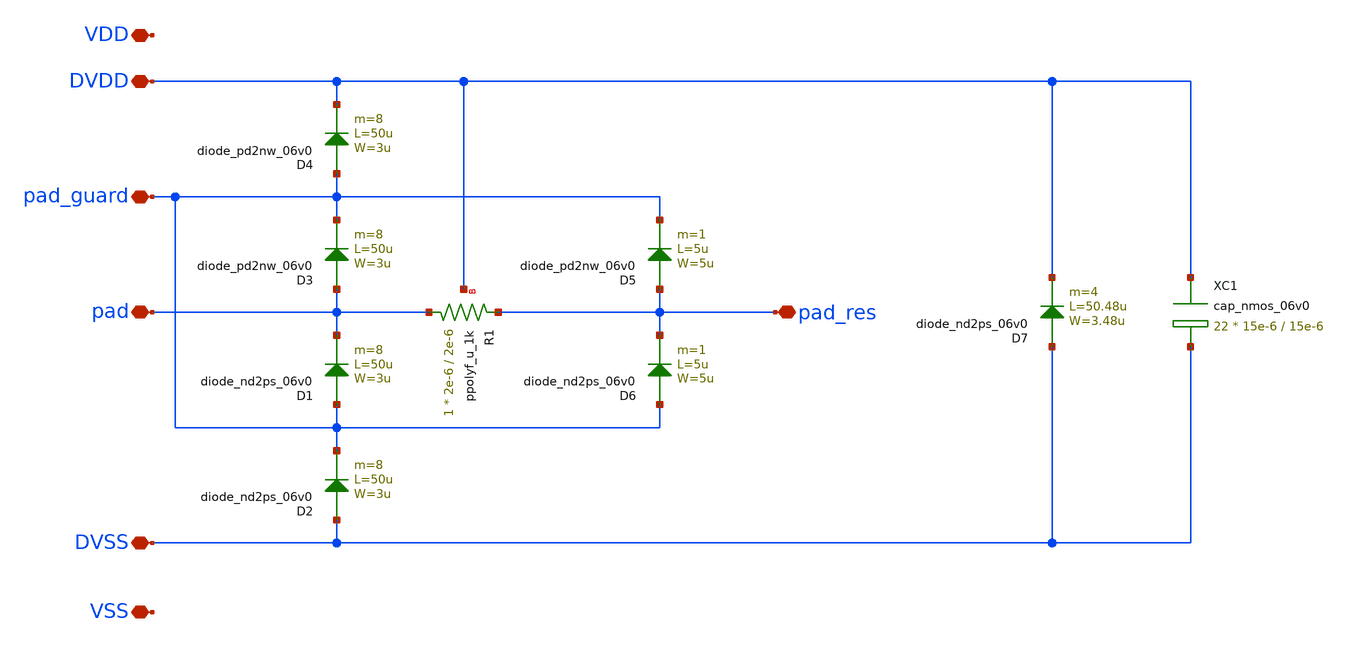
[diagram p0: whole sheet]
** sch_path: gf180mcuD/xschem/gf180mcu_liplib__asig_guard_5p0.sch
**.subckt gf180mcu_liplib__asig_guard_5p0 pad pad_guard DVDD DVSS pad_res VDD VSS
*.iopin pad
*.iopin pad_guard
*.iopin DVDD
*.iopin DVSS
*.iopin pad_res
*.iopin VDD
*.iopin VSS
D1 pad_guard pad diode_nd2ps_06v0 area='3u * 50u ' pj='2*3u + 2*50u ' m=8
D2 DVSS pad_guard diode_nd2ps_06v0 area='3u * 50u ' pj='2*3u + 2*50u ' m=8
D3 pad pad_guard diode_pd2nw_06v0 area='3u * 50u ' pj='2*3u + 2*50u ' m=8
D4 pad_guard DVDD diode_pd2nw_06v0 area='3u * 50u ' pj='2*3u + 2*50u ' m=8
XR1 pad pad_res DVDD ppolyf_u_1k r_width=2e-6 r_length=2e-6 m=1
D5 pad_res pad_guard diode_pd2nw_06v0 area='5u * 5u ' pj='2*5u + 2*5u ' m=1
D6 pad_guard pad_res diode_nd2ps_06v0 area='5u * 5u ' pj='2*5u + 2*5u ' m=1
D7 DVSS DVDD diode_nd2ps_06v0 area='3.48u * 50.48u ' pj='2*3.48u + 2*50.48u ' m=4
XC1 DVDD DVSS cap_nmos_06v0 c_width=15e-6 c_length=15e-6 m=22
**.ends
.end
